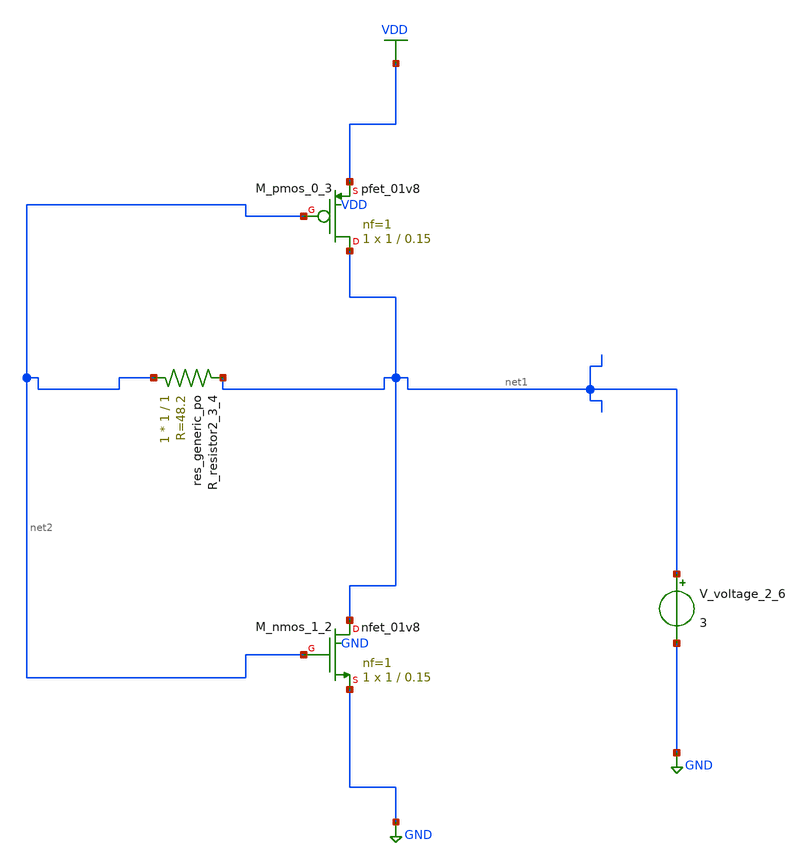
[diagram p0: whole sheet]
** sch_path: schematics/AMSNet/165.sch
**.subckt 165
XM_nmos_1_2 net1 net2 GND GND sky130_fd_pr__nfet_01v8 L=0.15 W=1 nf=1 ad='int((1 + 1)/2) * 1 / 1 * 0.29'
+ as='int((1 + 2)/2) * 1 / 1 * 0.29' pd='2*int((1 + 1)/2) * (1 / 1 + 0.29)' ps='2*int((1 + 2)/2) * (1 / 1 + 0.29)'
+ nrd='0.29 / 1 ' nrs='0.29 / 1 ' sa=0 sb=0 sd=0 mult=1 m=1
XM_pmos_0_3 net1 net2 VDD VDD sky130_fd_pr__pfet_01v8 L=0.15 W=1 nf=1 ad='int((1 + 1)/2) * 1 / 1 * 0.29'
+ as='int((1 + 2)/2) * 1 / 1 * 0.29' pd='2*int((1 + 1)/2) * (1 / 1 + 0.29)' ps='2*int((1 + 2)/2) * (1 / 1 + 0.29)'
+ nrd='0.29 / 1 ' nrs='0.29 / 1 ' sa=0 sb=0 sd=0 mult=1 m=1
XR_resistor2_3_4 net2 net1 sky130_fd_pr__res_generic_po W=1 L=1 m=1
V_voltage_2_6 net1 GND 3
**.ends
.GLOBAL GND
.GLOBAL VDD
.end
